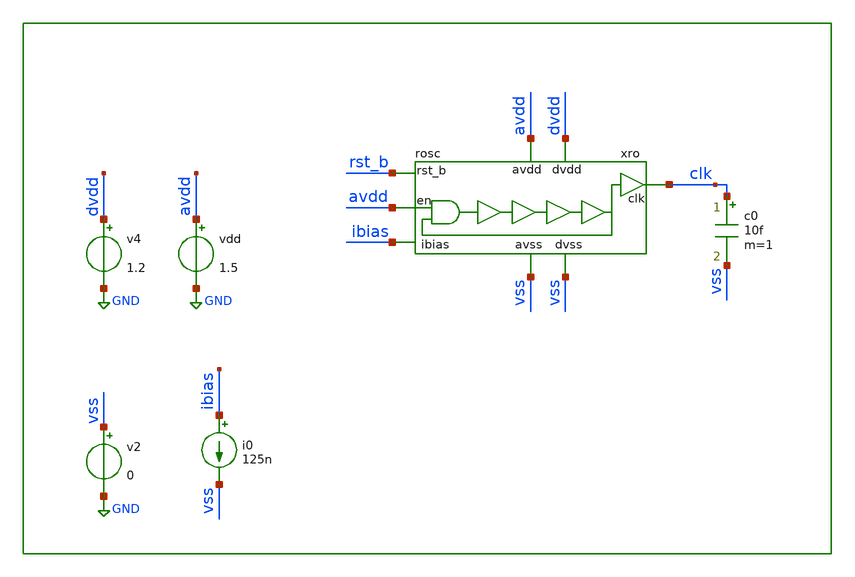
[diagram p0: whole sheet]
** sch_path: xschem/tb/rosc/tr_rosc.sch
**.subckt tr_rosc
c0 clk vss 10f m=1
i0 ibias vss 125n
xro avdd vss dvdd vss rst_b ibias clk avdd rosc
v2 vss GND 0
v4 dvdd GND 1.2
vdd avdd GND 1.5
**** begin user architecture code
.options method trap

.include $::DESIGN_PATH/rosc/rosc.pex.spice

ven  en    0  pulse(0 1.8 1u 1n 1n 100u 200u)
vre  rst_b 0  pulse(0 1.8 100n 1n 1n 100u 200u)

.control
.param MC_SWITCH=0
save all
tran 1e-9 10e-6
run
meas tran tclk TRIG clk val=0.5 td=7u rise=1 targ clk val=.5 td=7u rise=2
meas tran out_max max xro.out7 from=5u
meas tran out_min min xro.out7 from=5u
let fclk = 1/tclk
print out_max
print out_min
print fclk
.endc


* FET CORNERS
.include $::SKYWATER_MODELS/corners/tt.spice
*.include $::SKYWATER_MODELS/corners/ff.spice
*.include $::SKYWATER_MODELS/corners/ss.spice
*.include $::SKYWATER_MODELS/corners/sf.spice
*.include $::SKYWATER_MODELS/corners/fs.spice

* TT + R + C
*.include $::SKYWATER_MODELS/corners/tt_rmax_cmax.spice
*.include $::SKYWATER_MODELS/corners/tt_rmin_cmin.spice
*.include $::SKYWATER_MODELS/corners/tt_rmax_cmin.spice
*.include $::SKYWATER_MODELS/corners/tt_rmin_cmax.spice

* FF + R + C
*.include $::SKYWATER_MODELS/corners/ff_rmax_cmax.spice
*.include $::SKYWATER_MODELS/corners/ff_rmin_cmin.spice
*.include $::SKYWATER_MODELS/corners/ff_rmax_cmin.spice
*.include $::SKYWATER_MODELS/corners/ff_rmin_cmax.spice


* SS + R + C
*.include $::SKYWATER_MODELS/corners/ss_rmax_cmax.spice
*.include $::SKYWATER_MODELS/corners/ss_rmin_cmin.spice
*.include $::SKYWATER_MODELS/corners/ss_rmax_cmin.spice
*.include $::SKYWATER_MODELS/corners/ss_rmin_cmax.spice

* SF + R + C
*.include $::SKYWATER_MODELS/corners/sf_rmax_cmax.spice
*.include $::SKYWATER_MODELS/corners/sf_rmin_cmin.spice
*.include $::SKYWATER_MODELS/corners/sf_rmax_cmin.spice
*.include $::SKYWATER_MODELS/corners/sf_rmin_cmax.spice

* FS + R + C
*.include $::SKYWATER_MODELS/corners/fs_rmax_cmax.spice
*.include $::SKYWATER_MODELS/corners/fs_rmin_cmin.spice
*.include $::SKYWATER_MODELS/corners/fs_rmax_cmin.spice
*.include $::SKYWATER_MODELS/corners/fs_rmin_cmax.spice

**** end user architecture code
**.ends

* expanding   symbol:  rosc/rosc.sym # of pins=8
** sym_path: xschem/rosc/rosc.sym
** sch_path: xschem/rosc/rosc.sch
.subckt rosc avdd avss dvdd dvss rst_b ibias clk en
*.ipin en
*.iopin avss
*.opin clk
*.iopin dvdd
*.iopin dvss
*.iopin avdd
*.ipin rst_b
*.ipin ibias
x8 clk dvss dvss dvdd dvdd fb sky130_fd_sc_hd__inv_1
* noconn #net2
XM2 bias_n ibias avdd avdd sky130_fd_pr__pfet_01v8 L=1 W=1 nf=1 ad='int((nf+1)/2) * W/nf * 0.29' as='int((nf+2)/2) * W/nf * 0.29'
+ pd='2*int((nf+1)/2) * (W/nf + 0.29)' ps='2*int((nf+2)/2) * (W/nf + 0.29)' nrd='0.29 / W' nrs='0.29 / W'
+ sa=0 sb=0 sd=0 mult=16 m=16
XM1 ibias ibias avdd avdd sky130_fd_pr__pfet_01v8 L=1 W=1 nf=1 ad='int((nf+1)/2) * W/nf * 0.29' as='int((nf+2)/2) * W/nf * 0.29'
+ pd='2*int((nf+1)/2) * (W/nf + 0.29)' ps='2*int((nf+2)/2) * (W/nf + 0.29)' nrd='0.29 / W' nrs='0.29 / W'
+ sa=0 sb=0 sd=0 mult=4 m=4
x9 out_dig fb rst_b dvss dvss dvdd dvdd clk net2 sky130_fd_sc_hd__dfrbp_2
XM4 bias_n bias_n avss avss sky130_fd_pr__nfet_01v8 L=1 W=1 nf=1 ad='int((nf+1)/2) * W/nf * 0.29' as='int((nf+2)/2) * W/nf * 0.29'
+ pd='2*int((nf+1)/2) * (W/nf + 0.29)' ps='2*int((nf+2)/2) * (W/nf + 0.29)' nrd='0.29 / W' nrs='0.29 / W'
+ sa=0 sb=0 sd=0 mult=8 m=8
XM5 vn bias_n avss avss sky130_fd_pr__nfet_01v8 L=1 W=1 nf=1 ad='int((nf+1)/2) * W/nf * 0.29' as='int((nf+2)/2) * W/nf * 0.29'
+ pd='2*int((nf+1)/2) * (W/nf + 0.29)' ps='2*int((nf+2)/2) * (W/nf + 0.29)' nrd='0.29 / W' nrs='0.29 / W'
+ sa=0 sb=0 sd=0 mult=8 m=8
x7 out_ana dvss dvss dvdd dvdd out_dig sky130_fd_sc_hd__inv_1
XM3 vp ibias avdd avdd sky130_fd_pr__pfet_01v8 L=1 W=1 nf=1 ad='int((nf+1)/2) * W/nf * 0.29' as='int((nf+2)/2) * W/nf * 0.29'
+ pd='2*int((nf+1)/2) * (W/nf + 0.29)' ps='2*int((nf+2)/2) * (W/nf + 0.29)' nrd='0.29 / W' nrs='0.29 / W'
+ sa=0 sb=0 sd=0 mult=16 m=16
XC1 out1 avss sky130_fd_pr__cap_mim_m3_1 W=4 L=4 MF=1 m=1
XC2 out2 avss sky130_fd_pr__cap_mim_m3_1 W=4 L=4 MF=1 m=1
x6 avdd out7 out_ana avss inv_lvt
XM6 out2 out1 vn avss sky130_fd_pr__nfet_01v8_lvt L=0.4 W=1 nf=1 ad='int((nf+1)/2) * W/nf * 0.29' as='int((nf+2)/2) * W/nf * 0.29'
+ pd='2*int((nf+1)/2) * (W/nf + 0.29)' ps='2*int((nf+2)/2) * (W/nf + 0.29)' nrd='0.29 / W' nrs='0.29 / W'
+ sa=0 sb=0 sd=0 mult=1 m=1
XM7 out2 out1 vp avdd sky130_fd_pr__pfet_01v8_lvt L=0.4 W=1 nf=1 ad='int((nf+1)/2) * W/nf * 0.29' as='int((nf+2)/2) * W/nf * 0.29'
+ pd='2*int((nf+1)/2) * (W/nf + 0.29)' ps='2*int((nf+2)/2) * (W/nf + 0.29)' nrd='0.29 / W' nrs='0.29 / W'
+ sa=0 sb=0 sd=0 mult=1 m=1
XC3 out3 avss sky130_fd_pr__cap_mim_m3_1 W=4 L=4 MF=1 m=1
XC4 out4 avss sky130_fd_pr__cap_mim_m3_1 W=4 L=4 MF=1 m=1
XC5 out5 avss sky130_fd_pr__cap_mim_m3_1 W=4 L=4 MF=1 m=1
XC6 out6 avss sky130_fd_pr__cap_mim_m3_1 W=4 L=4 MF=1 m=1
XM18 net1 out7 vn avss sky130_fd_pr__nfet_01v8_lvt L=0.4 W=1 nf=1 ad='int((nf+1)/2) * W/nf * 0.29' as='int((nf+2)/2) * W/nf * 0.29'
+ pd='2*int((nf+1)/2) * (W/nf + 0.29)' ps='2*int((nf+2)/2) * (W/nf + 0.29)' nrd='0.29 / W' nrs='0.29 / W'
+ sa=0 sb=0 sd=0 mult=1 m=1
XM19 out1 en vp avdd sky130_fd_pr__pfet_01v8_lvt L=0.4 W=1 nf=1 ad='int((nf+1)/2) * W/nf * 0.29' as='int((nf+2)/2) * W/nf * 0.29'
+ pd='2*int((nf+1)/2) * (W/nf + 0.29)' ps='2*int((nf+2)/2) * (W/nf + 0.29)' nrd='0.29 / W' nrs='0.29 / W'
+ sa=0 sb=0 sd=0 mult=1 m=1
XM20 out1 en net1 avss sky130_fd_pr__nfet_01v8_lvt L=0.4 W=1 nf=1 ad='int((nf+1)/2) * W/nf * 0.29' as='int((nf+2)/2) * W/nf * 0.29'
+ pd='2*int((nf+1)/2) * (W/nf + 0.29)' ps='2*int((nf+2)/2) * (W/nf + 0.29)' nrd='0.29 / W' nrs='0.29 / W'
+ sa=0 sb=0 sd=0 mult=1 m=1
XM21 out1 out7 vp avdd sky130_fd_pr__pfet_01v8_lvt L=0.4 W=1 nf=1 ad='int((nf+1)/2) * W/nf * 0.29' as='int((nf+2)/2) * W/nf * 0.29'
+ pd='2*int((nf+1)/2) * (W/nf + 0.29)' ps='2*int((nf+2)/2) * (W/nf + 0.29)' nrd='0.29 / W' nrs='0.29 / W'
+ sa=0 sb=0 sd=0 mult=1 m=1
XM8 out3 out2 vn avss sky130_fd_pr__nfet_01v8_lvt L=0.4 W=1 nf=1 ad='int((nf+1)/2) * W/nf * 0.29' as='int((nf+2)/2) * W/nf * 0.29'
+ pd='2*int((nf+1)/2) * (W/nf + 0.29)' ps='2*int((nf+2)/2) * (W/nf + 0.29)' nrd='0.29 / W' nrs='0.29 / W'
+ sa=0 sb=0 sd=0 mult=1 m=1
XM9 out3 out2 vp avdd sky130_fd_pr__pfet_01v8_lvt L=0.4 W=1 nf=1 ad='int((nf+1)/2) * W/nf * 0.29' as='int((nf+2)/2) * W/nf * 0.29'
+ pd='2*int((nf+1)/2) * (W/nf + 0.29)' ps='2*int((nf+2)/2) * (W/nf + 0.29)' nrd='0.29 / W' nrs='0.29 / W'
+ sa=0 sb=0 sd=0 mult=1 m=1
XM10 out4 out3 vn avss sky130_fd_pr__nfet_01v8_lvt L=0.4 W=1 nf=1 ad='int((nf+1)/2) * W/nf * 0.29' as='int((nf+2)/2) * W/nf * 0.29'
+ pd='2*int((nf+1)/2) * (W/nf + 0.29)' ps='2*int((nf+2)/2) * (W/nf + 0.29)' nrd='0.29 / W' nrs='0.29 / W'
+ sa=0 sb=0 sd=0 mult=1 m=1
XM11 out4 out3 vp avdd sky130_fd_pr__pfet_01v8_lvt L=0.4 W=1 nf=1 ad='int((nf+1)/2) * W/nf * 0.29' as='int((nf+2)/2) * W/nf * 0.29'
+ pd='2*int((nf+1)/2) * (W/nf + 0.29)' ps='2*int((nf+2)/2) * (W/nf + 0.29)' nrd='0.29 / W' nrs='0.29 / W'
+ sa=0 sb=0 sd=0 mult=1 m=1
XM12 out5 out4 vn avss sky130_fd_pr__nfet_01v8_lvt L=0.4 W=1 nf=1 ad='int((nf+1)/2) * W/nf * 0.29' as='int((nf+2)/2) * W/nf * 0.29'
+ pd='2*int((nf+1)/2) * (W/nf + 0.29)' ps='2*int((nf+2)/2) * (W/nf + 0.29)' nrd='0.29 / W' nrs='0.29 / W'
+ sa=0 sb=0 sd=0 mult=1 m=1
XM13 out5 out4 vp avdd sky130_fd_pr__pfet_01v8_lvt L=0.4 W=1 nf=1 ad='int((nf+1)/2) * W/nf * 0.29' as='int((nf+2)/2) * W/nf * 0.29'
+ pd='2*int((nf+1)/2) * (W/nf + 0.29)' ps='2*int((nf+2)/2) * (W/nf + 0.29)' nrd='0.29 / W' nrs='0.29 / W'
+ sa=0 sb=0 sd=0 mult=1 m=1
XM14 out6 out5 vn avss sky130_fd_pr__nfet_01v8_lvt L=0.4 W=1 nf=1 ad='int((nf+1)/2) * W/nf * 0.29' as='int((nf+2)/2) * W/nf * 0.29'
+ pd='2*int((nf+1)/2) * (W/nf + 0.29)' ps='2*int((nf+2)/2) * (W/nf + 0.29)' nrd='0.29 / W' nrs='0.29 / W'
+ sa=0 sb=0 sd=0 mult=1 m=1
XM15 out6 out5 vp avdd sky130_fd_pr__pfet_01v8_lvt L=0.4 W=1 nf=1 ad='int((nf+1)/2) * W/nf * 0.29' as='int((nf+2)/2) * W/nf * 0.29'
+ pd='2*int((nf+1)/2) * (W/nf + 0.29)' ps='2*int((nf+2)/2) * (W/nf + 0.29)' nrd='0.29 / W' nrs='0.29 / W'
+ sa=0 sb=0 sd=0 mult=1 m=1
XM16 out7 out6 vn avss sky130_fd_pr__nfet_01v8_lvt L=0.4 W=1 nf=1 ad='int((nf+1)/2) * W/nf * 0.29' as='int((nf+2)/2) * W/nf * 0.29'
+ pd='2*int((nf+1)/2) * (W/nf + 0.29)' ps='2*int((nf+2)/2) * (W/nf + 0.29)' nrd='0.29 / W' nrs='0.29 / W'
+ sa=0 sb=0 sd=0 mult=1 m=1
XM17 out7 out6 vp avdd sky130_fd_pr__pfet_01v8_lvt L=0.4 W=1 nf=1 ad='int((nf+1)/2) * W/nf * 0.29' as='int((nf+2)/2) * W/nf * 0.29'
+ pd='2*int((nf+1)/2) * (W/nf + 0.29)' ps='2*int((nf+2)/2) * (W/nf + 0.29)' nrd='0.29 / W' nrs='0.29 / W'
+ sa=0 sb=0 sd=0 mult=1 m=1
XC7 out7 avss sky130_fd_pr__cap_mim_m3_1 W=4 L=4 MF=1 m=1
.ends


* expanding   symbol:  logic/inv_lvt.sym # of pins=4
** sym_path: xschem/logic/inv_lvt.sym
** sch_path: xschem/logic/inv_lvt.sch
.subckt inv_lvt vdd in out vss
*.iopin vdd
*.iopin vss
*.ipin in
*.opin out
XM1 out in vss vss sky130_fd_pr__nfet_01v8_lvt L=0.4 W=1 nf=1 ad='int((nf+1)/2) * W/nf * 0.29' as='int((nf+2)/2) * W/nf * 0.29'
+ pd='2*int((nf+1)/2) * (W/nf + 0.29)' ps='2*int((nf+2)/2) * (W/nf + 0.29)' nrd='0.29 / W' nrs='0.29 / W'
+ sa=0 sb=0 sd=0 mult=1 m=1
XM2 out in vdd vdd sky130_fd_pr__pfet_01v8_lvt L=0.4 W=1 nf=1 ad='int((nf+1)/2) * W/nf * 0.29' as='int((nf+2)/2) * W/nf * 0.29'
+ pd='2*int((nf+1)/2) * (W/nf + 0.29)' ps='2*int((nf+2)/2) * (W/nf + 0.29)' nrd='0.29 / W' nrs='0.29 / W'
+ sa=0 sb=0 sd=0 mult=1 m=1
.ends

.GLOBAL GND
**** begin user architecture code
[sky130_models]

**** end user architecture code
.end
